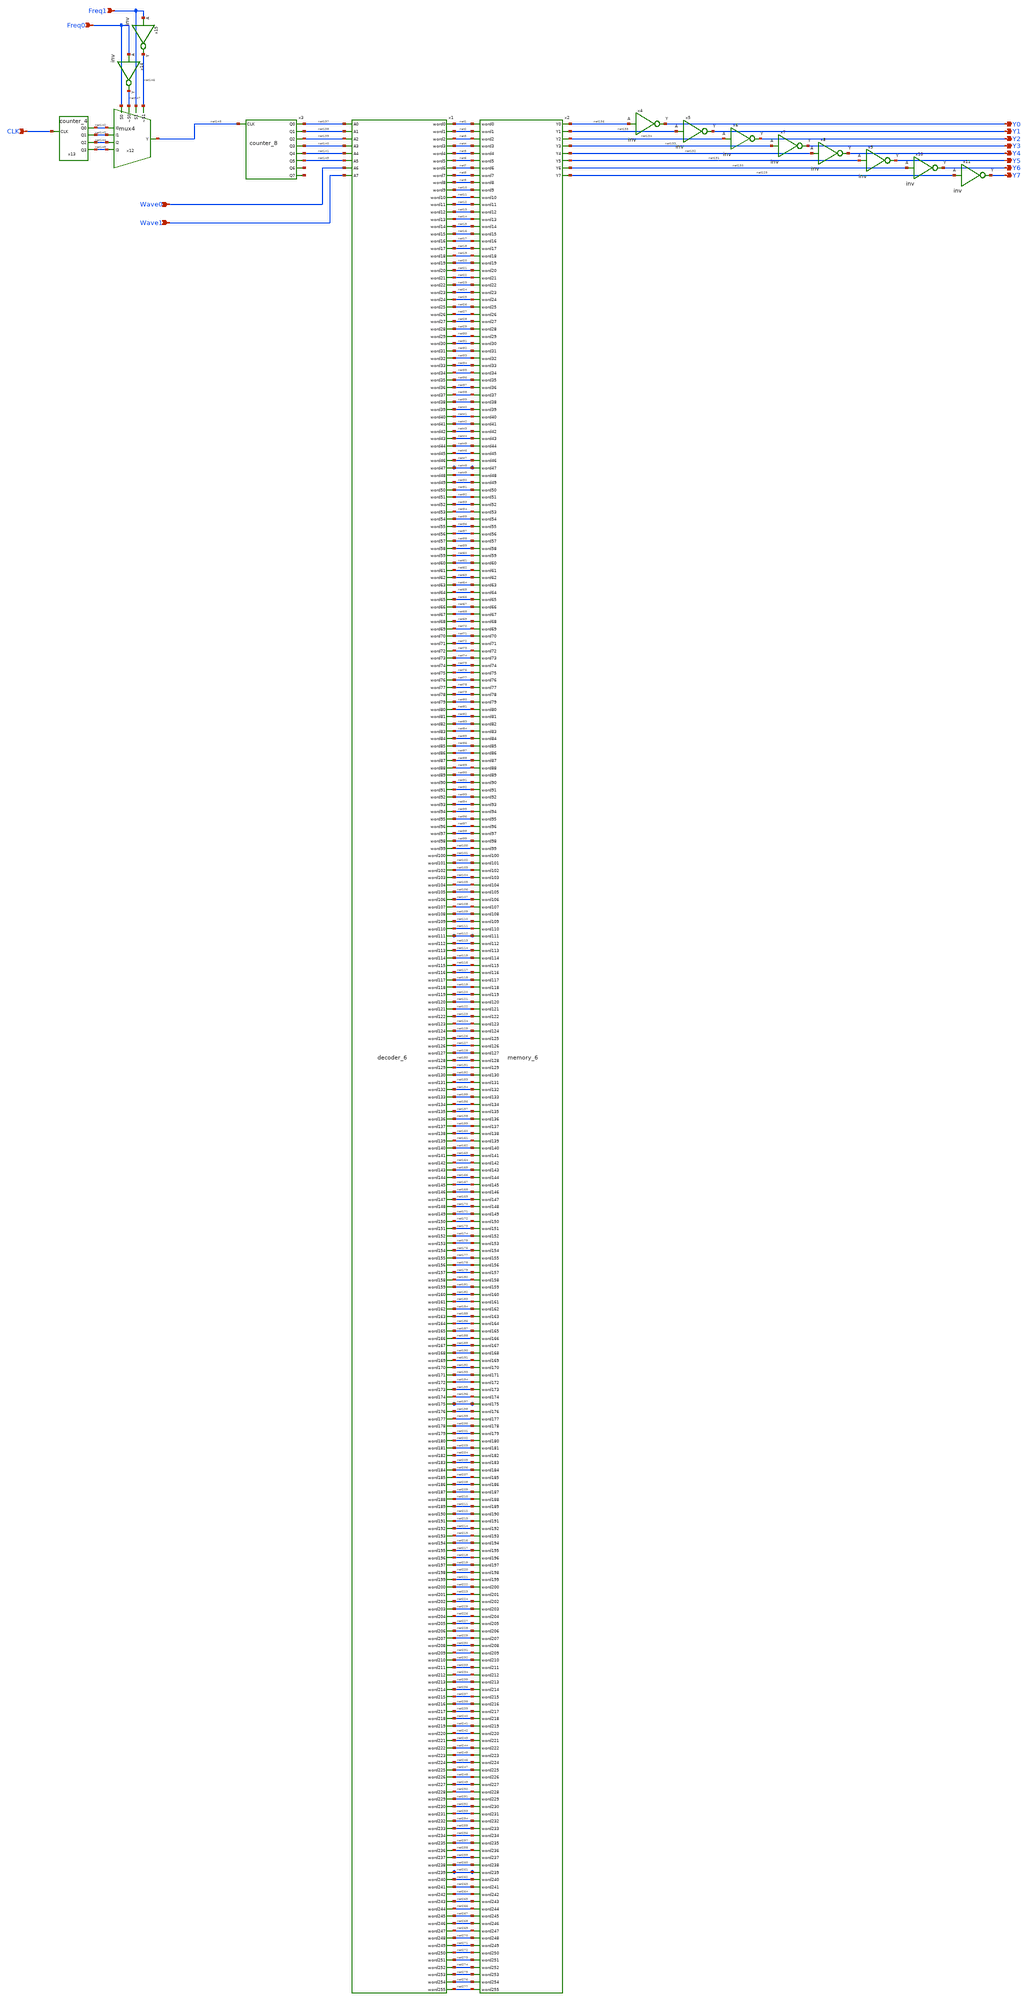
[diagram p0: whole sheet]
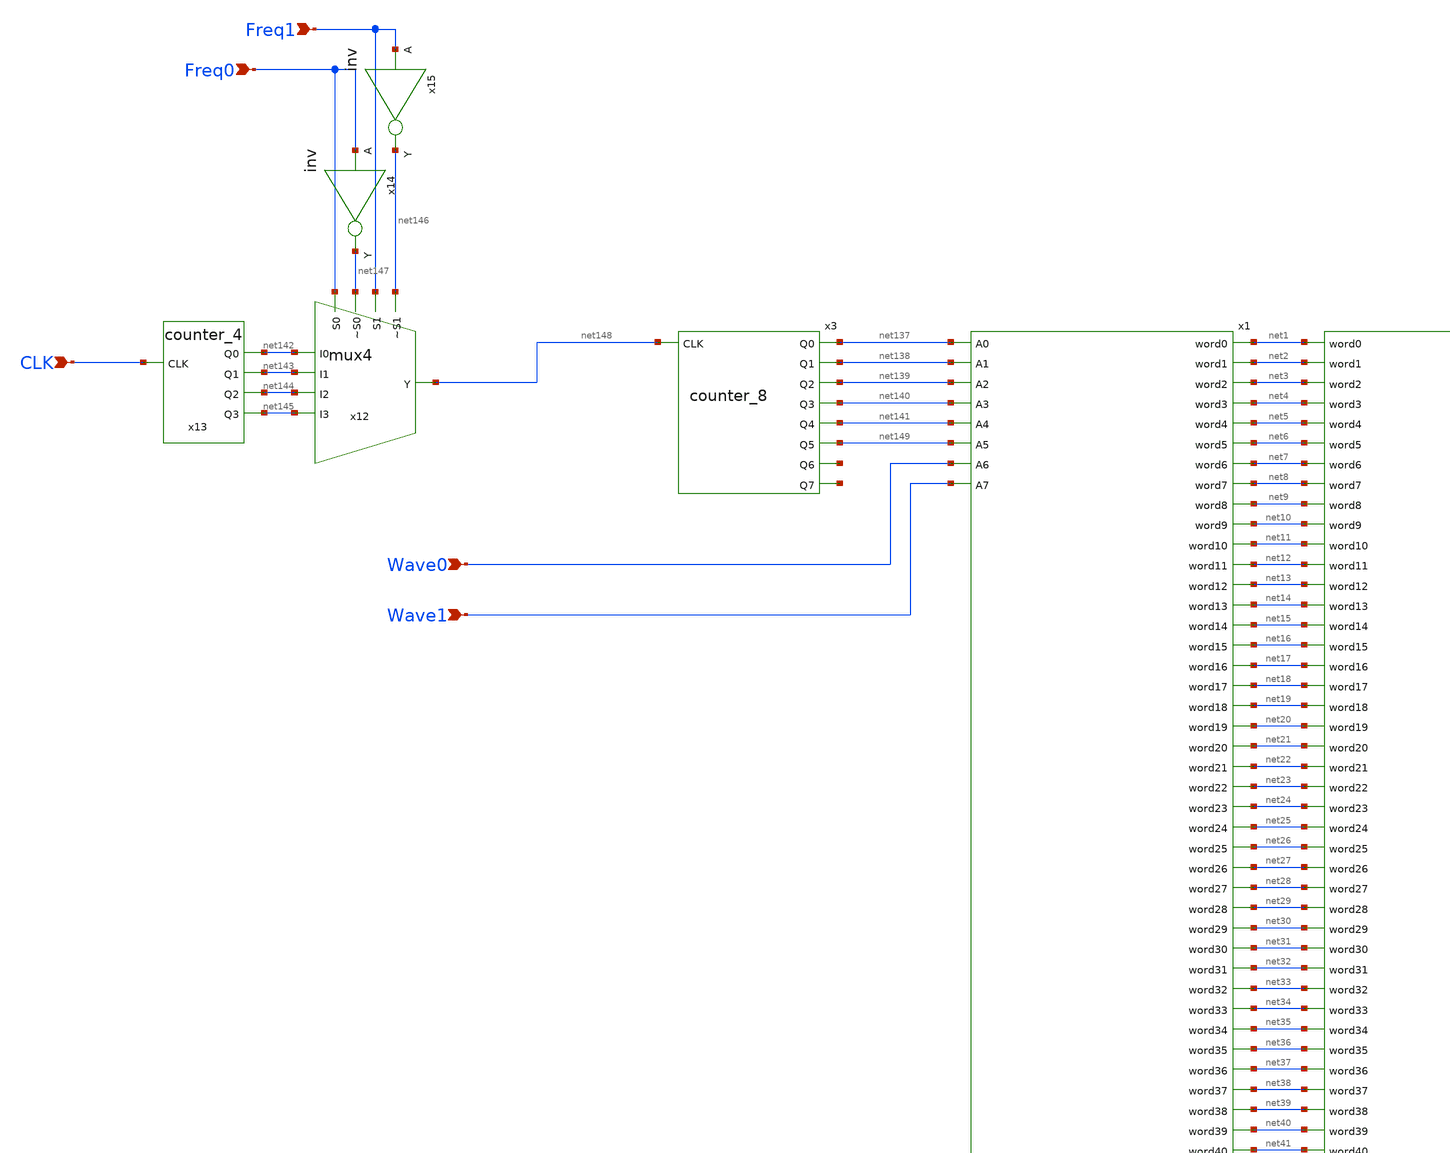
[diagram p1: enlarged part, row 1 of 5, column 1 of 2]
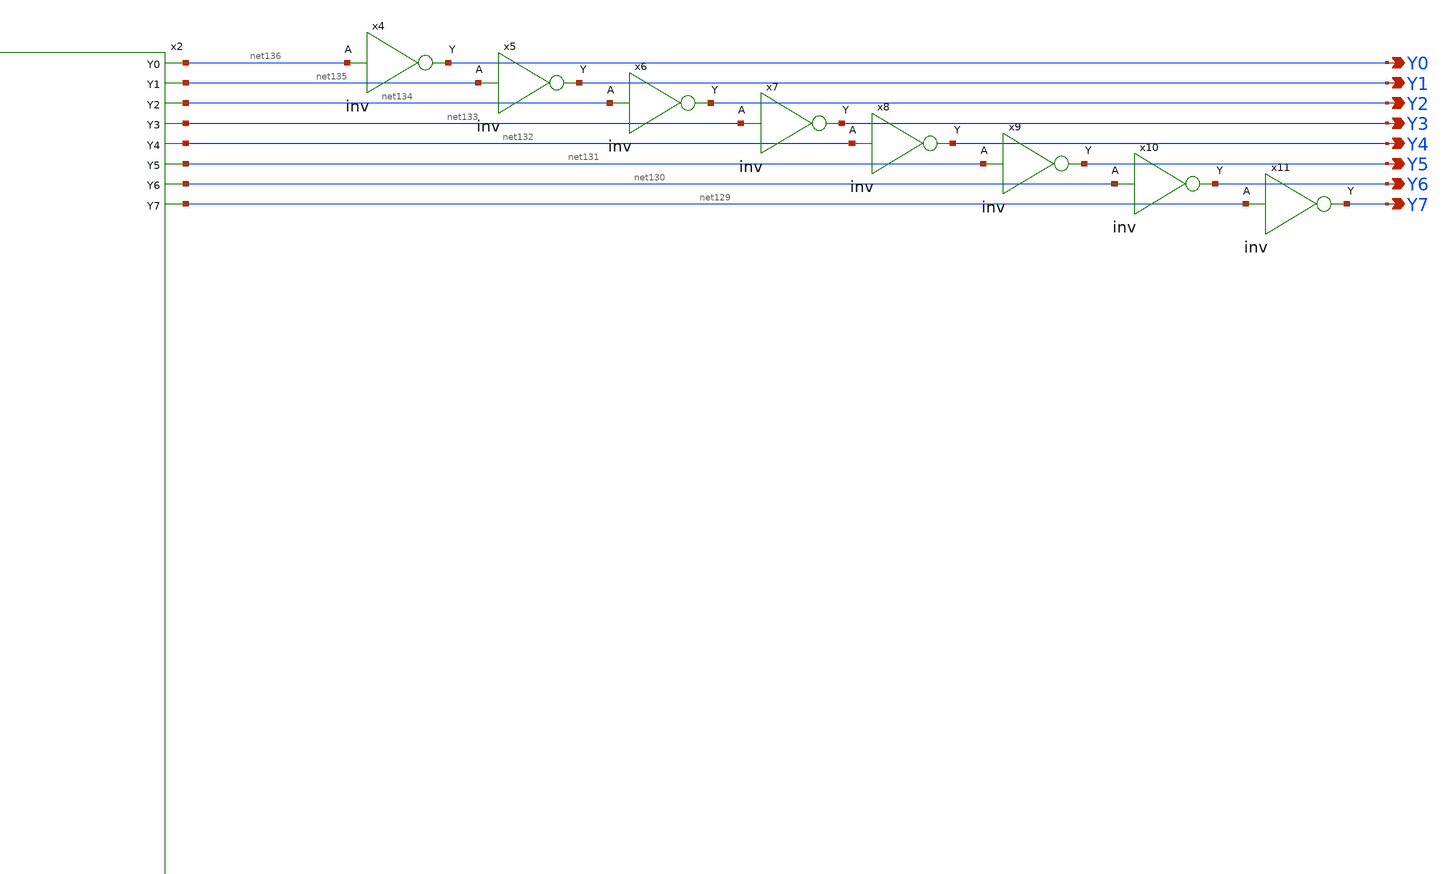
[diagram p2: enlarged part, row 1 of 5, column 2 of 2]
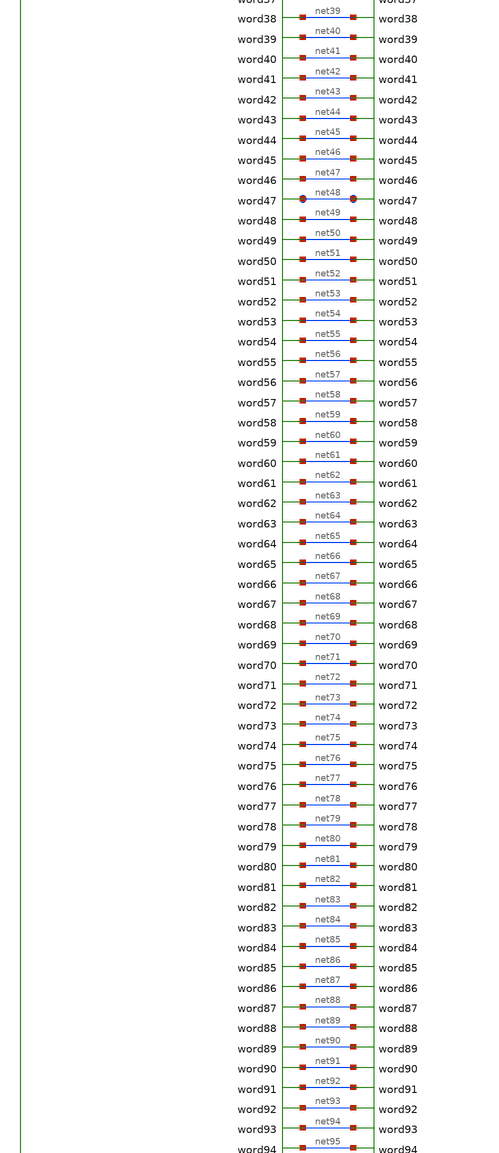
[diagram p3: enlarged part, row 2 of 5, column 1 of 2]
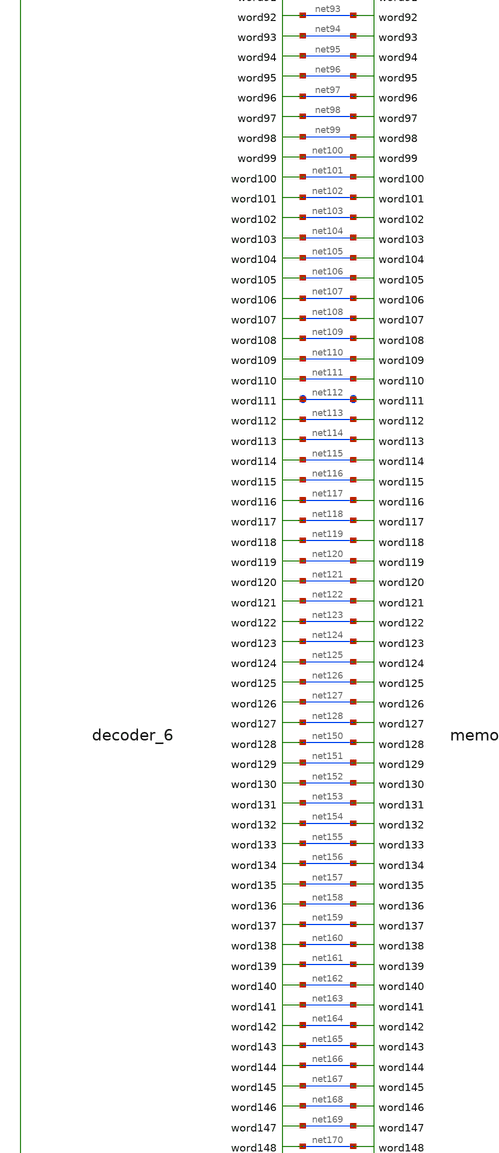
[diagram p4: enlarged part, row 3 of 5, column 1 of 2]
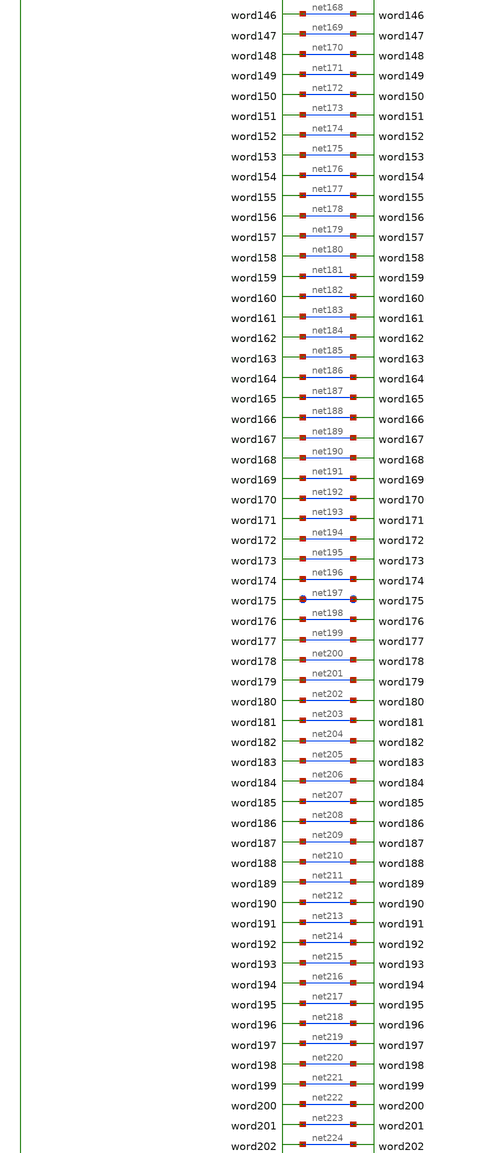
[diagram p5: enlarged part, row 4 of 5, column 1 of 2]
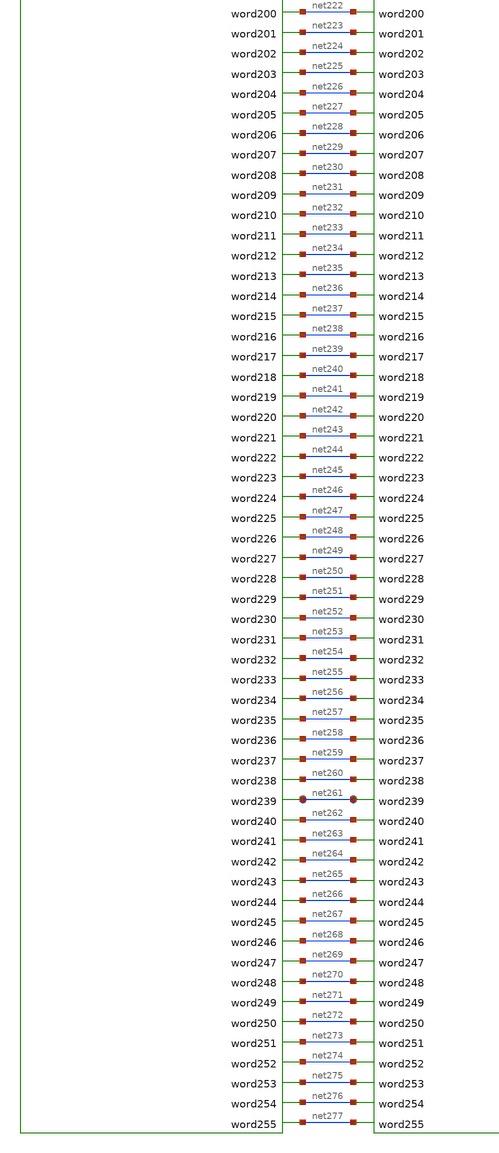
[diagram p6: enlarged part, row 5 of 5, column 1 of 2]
** sch_path: circuits/xschem/func_gen_6.sch
**.subckt func_gen_6 CLK Freq0 Freq1 Y0 Y1 Y2 Y3 Y4 Y5 Y6 Y7 Wave0 Wave1
*.ipin CLK
*.ipin Freq0
*.ipin Freq1
*.opin Y0
*.opin Y1
*.opin Y2
*.opin Y3
*.opin Y4
*.opin Y5
*.opin Y6
*.opin Y7
*.ipin Wave0
*.ipin Wave1
x3 net137 net138 net139 net140 net141 net149 net278 net279 net148 counter_8
x4 Y0 net136 inv
x5 Y1 net135 inv
x6 Y2 net134 inv
x7 Y3 net133 inv
x8 Y4 net132 inv
x9 Y5 net131 inv
x10 Y6 net130 inv
x11 Y7 net129 inv
x12 Freq0 net147 Freq1 net146 net142 net143 net148 net144 net145 mux4
x13 net142 net143 net144 net145 CLK counter_4
x14 net147 Freq0 inv
x15 net146 Freq1 inv
x1 net138 net139 net140 net141 net149 Wave0 Wave1 net137 net1 net2 net3 net4 net5 net6 net7 net8
+ net9 net10 net11 net12 net13 net14 net15 net16 net17 net18 net19 net20 net21 net22 net23 net24 net25
+ net26 net27 net28 net29 net30 net31 net32 net33 net34 net35 net36 net37 net38 net39 net40 net41 net42
+ net43 net44 net45 net46 net47 net48 net49 net50 net51 net52 net53 net54 net55 net56 net57 net58 net59
+ net60 net61 net62 net63 net64 net65 net66 net67 net68 net69 net70 net71 net72 net73 net74 net75 net76
+ net77 net78 net79 net80 net81 net82 net83 net84 net85 net86 net87 net88 net89 net90 net91 net92 net93
+ net94 net95 net96 net97 net98 net99 net100 net101 net102 net103 net104 net105 net106 net107 net108 net109
+ net110 net111 net112 net113 net114 net115 net116 net117 net118 net119 net120 net121 net122 net123 net124
+ net125 net126 net127 net128 net150 net151 net152 net153 net154 net155 net156 net157 net158 net159 net160
+ net161 net162 net163 net164 net165 net166 net167 net168 net169 net170 net171 net172 net173 net174 net175
+ net176 net177 net178 net179 net180 net181 net182 net183 net184 net185 net186 net187 net188 net189 net190
+ net191 net192 net193 net194 net195 net196 net197 net198 net199 net200 net201 net202 net203 net204 net205
+ net206 net207 net208 net209 net210 net211 net212 net213 net214 net215 net216 net217 net218 net219 net220
+ net221 net222 net223 net224 net225 net226 net227 net228 net229 net230 net231 net232 net233 net234 net235
+ net236 net237 net238 net239 net240 net241 net242 net243 net244 net245 net246 net247 net248 net249 net250
+ net251 net252 net253 net254 net255 net256 net257 net258 net259 net260 net261 net262 net263 net264 net265
+ net266 net267 net268 net269 net270 net271 net272 net273 net274 net275 net276 net277 decoder_6
x2 net1 net2 net3 net4 net5 net6 net7 net8 net9 net10 net11 net12 net13 net14 net15 net16 net17
+ net18 net19 net20 net21 net22 net23 net24 net25 net26 net27 net28 net29 net30 net31 net32 net33 net34
+ net35 net36 net37 net38 net39 net40 net41 net42 net43 net44 net45 net46 net47 net48 net49 net50 net51
+ net52 net53 net54 net55 net56 net57 net58 net59 net60 net61 net62 net63 net64 net65 net66 net67 net68
+ net69 net70 net71 net72 net73 net74 net75 net76 net77 net78 net79 net80 net81 net82 net83 net84 net85
+ net86 net87 net88 net89 net90 net91 net92 net93 net94 net95 net96 net97 net98 net99 net100 net101 net102
+ net103 net104 net105 net106 net107 net108 net109 net110 net111 net112 net113 net114 net115 net116 net117
+ net118 net119 net120 net121 net122 net123 net124 net125 net126 net127 net128 net150 net151 net152 net153
+ net154 net155 net156 net157 net158 net159 net160 net161 net162 net163 net164 net165 net166 net167 net168
+ net169 net170 net171 net172 net173 net174 net175 net176 net177 net178 net179 net180 net181 net182 net183
+ net184 net185 net186 net187 net188 net189 net190 net191 net192 net193 net194 net195 net196 net197 net198
+ net199 net200 net201 net202 net203 net204 net205 net206 net207 net208 net209 net210 net211 net212 net213
+ net214 net215 net216 net217 net218 net219 net220 net221 net222 net223 net224 net225 net226 net227 net228
+ net229 net230 net231 net232 net233 net234 net235 net236 net237 net238 net239 net240 net241 net242 net243
+ net244 net245 net246 net247 net248 net249 net250 net251 net252 net253 net254 net255 net256 net257 net258
+ net259 net260 net261 net262 net263 net264 net265 net266 net267 net268 net269 net270 net271 net272 net273
+ net274 net275 net276 net277 net136 net135 net134 net133 net132 net131 net130 net129 memory_6
**.ends
.end
